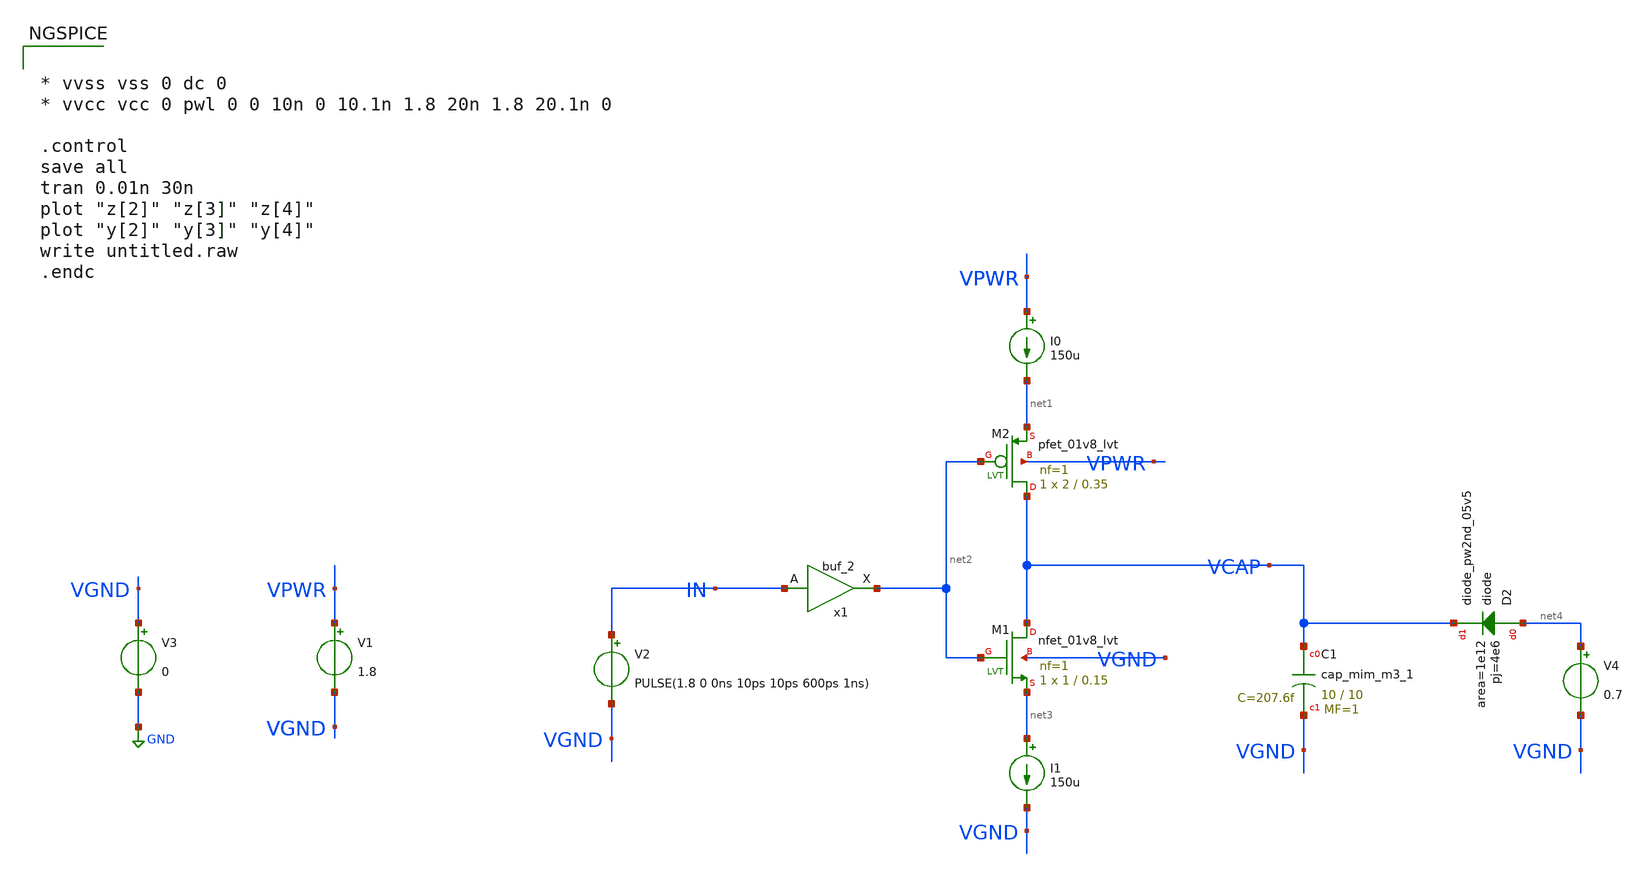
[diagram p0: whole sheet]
** sch_path: design/untitled.sch
**.subckt untitled
XM1 VCAP net2 net3 VGND sky130_fd_pr__nfet_01v8_lvt L=0.15 W=1 nf=1 ad='int((nf+1)/2) * W/nf * 0.29'
+ as='int((nf+2)/2) * W/nf * 0.29' pd='2*int((nf+1)/2) * (W/nf + 0.29)' ps='2*int((nf+2)/2) * (W/nf + 0.29)'
+ nrd='0.29 / W' nrs='0.29 / W' sa=0 sb=0 sd=0 mult=1 m=1
XM2 VCAP net2 net1 VPWR sky130_fd_pr__pfet_01v8_lvt L=0.35 W=2 nf=1 ad='int((nf+1)/2) * W/nf * 0.29'
+ as='int((nf+2)/2) * W/nf * 0.29' pd='2*int((nf+1)/2) * (W/nf + 0.29)' ps='2*int((nf+2)/2) * (W/nf + 0.29)'
+ nrd='0.29 / W' nrs='0.29 / W' sa=0 sb=0 sd=0 mult=1 m=1
x1 IN VGND VNB VPB VPWR net2 sky130_fd_sc_hd__buf_2
I0 VPWR net1 150u
I1 net3 VGND 150u
XC1 VCAP VGND sky130_fd_pr__cap_mim_m3_1 W=10 L=10 MF=1 m=1
V1 VPWR VGND 1.8
V2 IN VGND PULSE(1.8 0 0ns 10ps 10ps 600ps 1ns)
V3 VGND GND 0
V4 net4 VGND 0.7
XD2 net4 VCAP sky130_fd_pr__diode_pw2nd_05v5 area=1e12 pj=4e6
**** begin user architecture code

** opencircuitdesign pdks install
*.lib sky130.lib.spice tt_mm
.lib /farmshare/home/classes/ee/372/PDKs/open_pdks/sky130/sky130A/libs.tech/ngspice/sky130.lib.spice tt
.include /farmshare/home/classes/ee/372/PDKs/open_pdks/sky130/sky130A/libs.ref/sky130_fd_sc_hd/spice/sky130_fd_sc_hd.spice




* vvss vss 0 dc 0
* vvcc vcc 0 pwl 0 0 10n 0 10.1n 1.8 20n 1.8 20.1n 0

.control
save all
tran 0.01n 30n
plot "z[2]" "z[3]" "z[4]"
plot "y[2]" "y[3]" "y[4]"
write untitled.raw
.endc


**** end user architecture code
**.ends
.GLOBAL GND
.end
